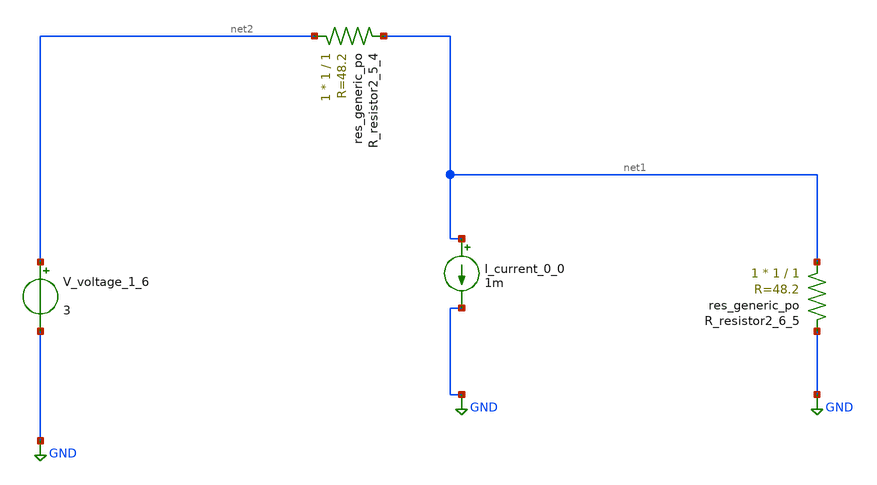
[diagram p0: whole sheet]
** sch_path: schematics/AMSNet/788.sch
**.subckt 788
I_current_0_0 net1 GND 1m
XR_resistor2_5_4 net2 net1 sky130_fd_pr__res_generic_po W=1 L=1 m=1
XR_resistor2_6_5 net1 GND sky130_fd_pr__res_generic_po W=1 L=1 m=1
V_voltage_1_6 net2 GND 3
**.ends
.GLOBAL GND
.end
